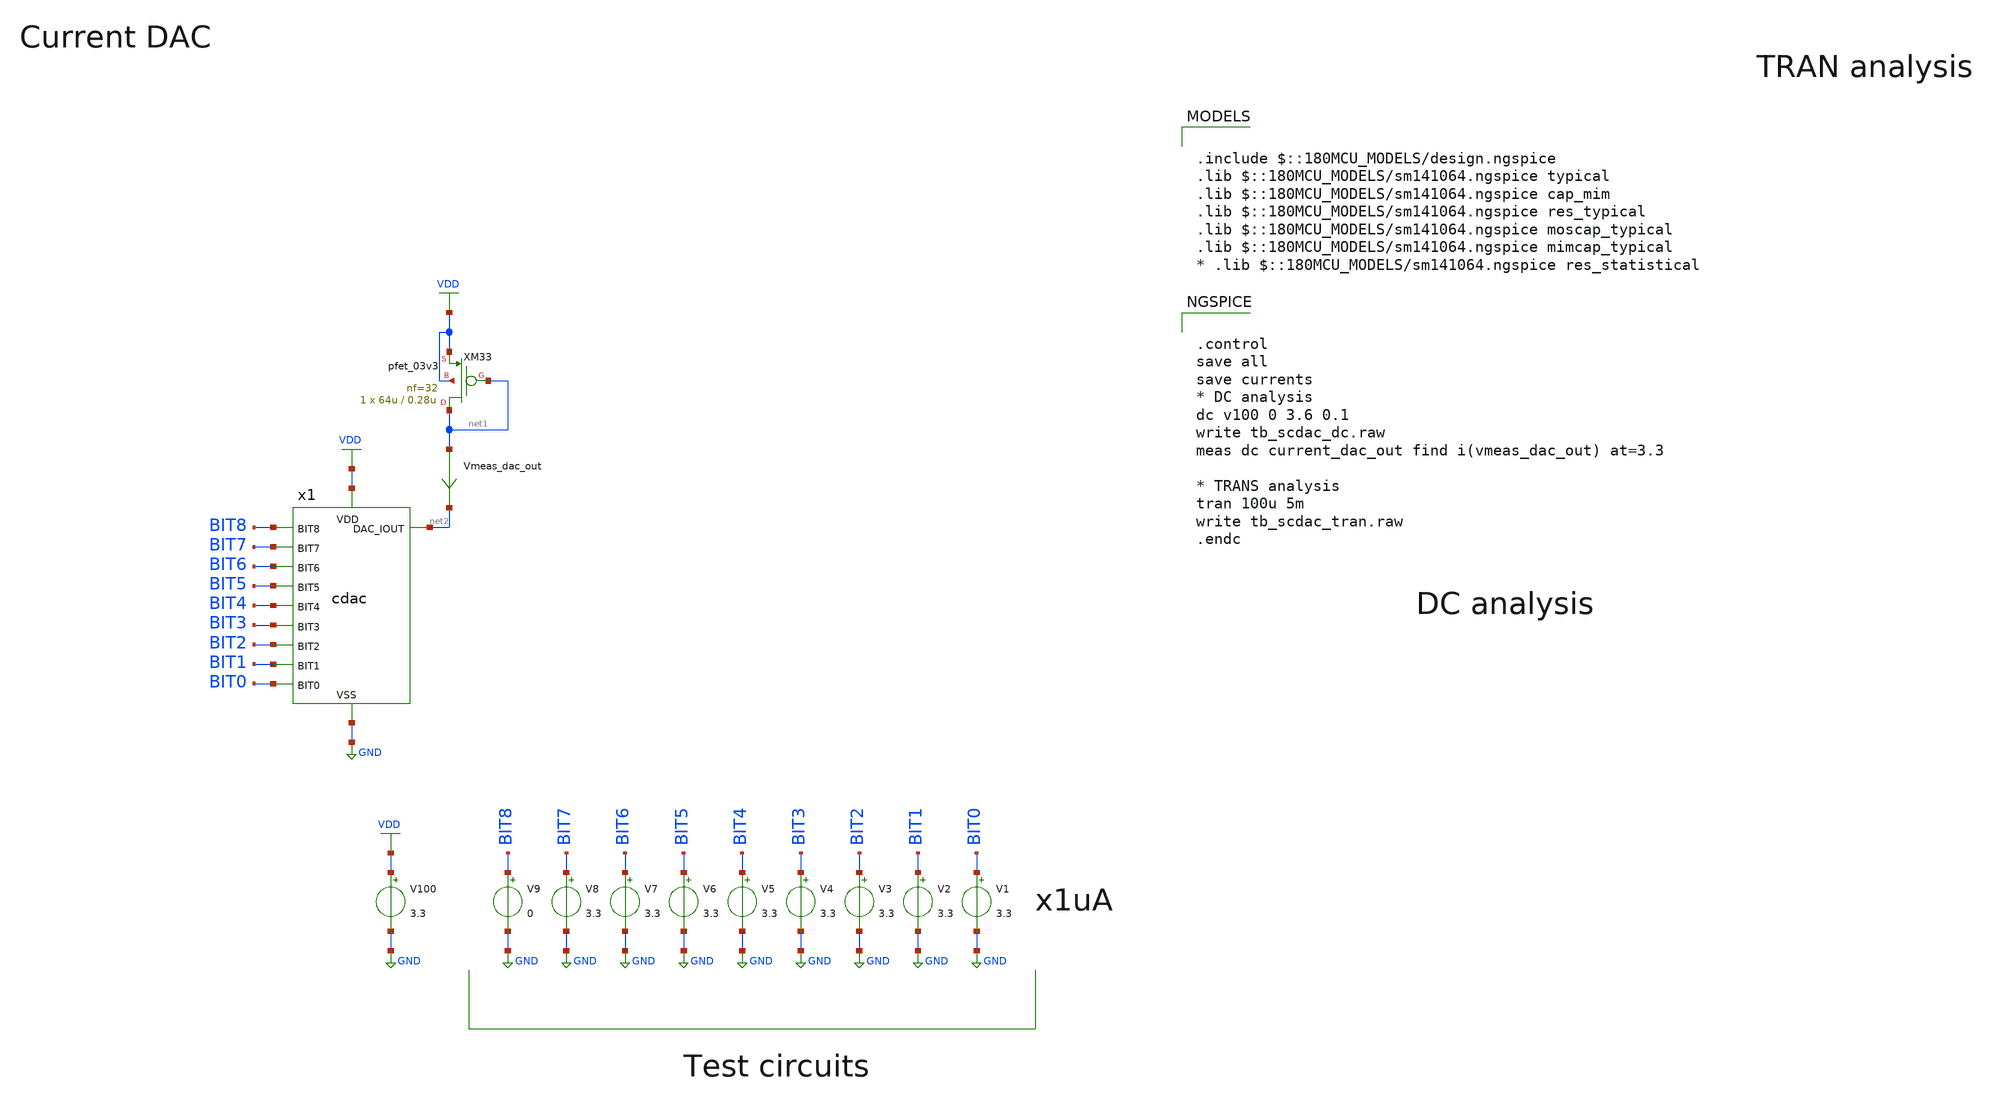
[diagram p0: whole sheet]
** sch_path: designs/libs/tb_analog/tb_scdac/tb_scdac.sch
* Copyright 2022 GlobalFoundries PDK Authors
* Licensed under the Apache License, Version 2.0 (the "License");
* you may not use this file except in compliance with the License.
* You may obtain a copy of the License at
* https://www.apache.org/licenses/LICENSE-2.0
* Unless required by applicable law or agreed to in writing, software
* distributed under the License is distributed on an "AS IS" BASIS,
* WITHOUT WARRANTIES OR CONDITIONS OF ANY KIND, either express or implied.
* See the License for the specific language governing permissions and
* limitations under the License.
**.subckt tb_scdac
V100 VDD GND 3.3
XM33 net1 net1 VDD VDD pfet_03v3 L=0.28u W=64u nf=32 ad='int((nf+1)/2) * W/nf * 0.18u' as='int((nf+2)/2) * W/nf * 0.18u'
+ pd='2*int((nf+1)/2) * (W/nf + 0.18u)' ps='2*int((nf+2)/2) * (W/nf + 0.18u)' nrd='0.18u / W' nrs='0.18u / W'
+ sa=0 sb=0 sd=0 m=1
Vmeas_dac_out net1 net2 0
.save i(vmeas_dac_out)
V8 BIT7 GND 3.3
V7 BIT6 GND 3.3
V6 BIT5 GND 3.3
V5 BIT4 GND 3.3
V4 BIT3 GND 3.3
V3 BIT2 GND 3.3
V2 BIT1 GND 3.3
V1 BIT0 GND 3.3
V9 BIT8 GND 0
x1 net2 GND VDD BIT8 BIT7 BIT6 BIT5 BIT4 BIT3 BIT2 BIT1 BIT0 cdac
**** begin user architecture code


.control
save all
save currents
* DC analysis
dc v100 0 3.6 0.1
write tb_scdac_dc.raw
meas dc current_dac_out find i(vmeas_dac_out) at=3.3

* TRANS analysis
tran 100u 5m
write tb_scdac_tran.raw
.endc



.include $::180MCU_MODELS/design.ngspice
.lib $::180MCU_MODELS/sm141064.ngspice typical
.lib $::180MCU_MODELS/sm141064.ngspice cap_mim
.lib $::180MCU_MODELS/sm141064.ngspice res_typical
.lib $::180MCU_MODELS/sm141064.ngspice moscap_typical
.lib $::180MCU_MODELS/sm141064.ngspice mimcap_typical
* .lib $::180MCU_MODELS/sm141064.ngspice res_statistical

**** end user architecture code
**.ends

* expanding   symbol:  libs/core_analog/scdac/cdac.sym # of pins=12
** sym_path: designs/libs/core_analog/scdac/cdac.sym
** sch_path: designs/libs/core_analog/scdac/cdac.sch
.subckt cdac DAC_IOUT VSS VDD BIT8 BIT7 BIT6 BIT5 BIT4 BIT3 BIT2 BIT1 BIT0
*.ipin BIT8
*.ipin BIT7
*.ipin BIT6
*.ipin BIT5
*.ipin BIT4
*.ipin BIT3
*.ipin BIT2
*.ipin BIT1
*.ipin BIT0
*.ipin VDD
*.ipin VSS
*.opin DAC_IOUT
XM8 64uA_REF 64uA_REF VSS VSS nfet_03v3 L=1u W=64u nf=1 ad='int((nf+1)/2) * W/nf * 0.18u' as='int((nf+2)/2) * W/nf * 0.18u'
+ pd='2*int((nf+1)/2) * (W/nf + 0.18u)' ps='2*int((nf+2)/2) * (W/nf + 0.18u)' nrd='0.18u / W' nrs='0.18u / W'
+ sa=0 sb=0 sd=0 m=1
XM11 net1 64uA_REF VSS VSS nfet_03v3 L=1u W=61.1u nf=1 ad='int((nf+1)/2) * W/nf * 0.18u' as='int((nf+2)/2) * W/nf * 0.18u'
+ pd='2*int((nf+1)/2) * (W/nf + 0.18u)' ps='2*int((nf+2)/2) * (W/nf + 0.18u)' nrd='0.18u / W' nrs='0.18u / W'
+ sa=0 sb=0 sd=0 m=1
XM13 DAC_IOUT BIT8 net1 VSS nfet_03v3 L=0.28u W=4u nf=1 ad='int((nf+1)/2) * W/nf * 0.18u' as='int((nf+2)/2) * W/nf * 0.18u'
+ pd='2*int((nf+1)/2) * (W/nf + 0.18u)' ps='2*int((nf+2)/2) * (W/nf + 0.18u)' nrd='0.18u / W' nrs='0.18u / W'
+ sa=0 sb=0 sd=0 m=1
XM15 net2 64uA_REF VSS VSS nfet_03v3 L=1u W=61.1u nf=1 ad='int((nf+1)/2) * W/nf * 0.18u' as='int((nf+2)/2) * W/nf * 0.18u'
+ pd='2*int((nf+1)/2) * (W/nf + 0.18u)' ps='2*int((nf+2)/2) * (W/nf + 0.18u)' nrd='0.18u / W' nrs='0.18u / W'
+ sa=0 sb=0 sd=0 m=1
XM16 DAC_IOUT BIT8 net2 VSS nfet_03v3 L=0.28u W=4u nf=1 ad='int((nf+1)/2) * W/nf * 0.18u' as='int((nf+2)/2) * W/nf * 0.18u'
+ pd='2*int((nf+1)/2) * (W/nf + 0.18u)' ps='2*int((nf+2)/2) * (W/nf + 0.18u)' nrd='0.18u / W' nrs='0.18u / W'
+ sa=0 sb=0 sd=0 m=1
XM18 net3 64uA_REF VSS VSS nfet_03v3 L=1u W=61.1u nf=1 ad='int((nf+1)/2) * W/nf * 0.18u' as='int((nf+2)/2) * W/nf * 0.18u'
+ pd='2*int((nf+1)/2) * (W/nf + 0.18u)' ps='2*int((nf+2)/2) * (W/nf + 0.18u)' nrd='0.18u / W' nrs='0.18u / W'
+ sa=0 sb=0 sd=0 m=1
XM19 DAC_IOUT BIT8 net3 VSS nfet_03v3 L=0.28u W=4u nf=1 ad='int((nf+1)/2) * W/nf * 0.18u' as='int((nf+2)/2) * W/nf * 0.18u'
+ pd='2*int((nf+1)/2) * (W/nf + 0.18u)' ps='2*int((nf+2)/2) * (W/nf + 0.18u)' nrd='0.18u / W' nrs='0.18u / W'
+ sa=0 sb=0 sd=0 m=1
XM21 net4 64uA_REF VSS VSS nfet_03v3 L=1u W=61.1u nf=1 ad='int((nf+1)/2) * W/nf * 0.18u' as='int((nf+2)/2) * W/nf * 0.18u'
+ pd='2*int((nf+1)/2) * (W/nf + 0.18u)' ps='2*int((nf+2)/2) * (W/nf + 0.18u)' nrd='0.18u / W' nrs='0.18u / W'
+ sa=0 sb=0 sd=0 m=1
XM22 DAC_IOUT BIT8 net4 VSS nfet_03v3 L=0.28u W=4u nf=1 ad='int((nf+1)/2) * W/nf * 0.18u' as='int((nf+2)/2) * W/nf * 0.18u'
+ pd='2*int((nf+1)/2) * (W/nf + 0.18u)' ps='2*int((nf+2)/2) * (W/nf + 0.18u)' nrd='0.18u / W' nrs='0.18u / W'
+ sa=0 sb=0 sd=0 m=1
XM24 net5 64uA_REF VSS VSS nfet_03v3 L=1u W=61.1u nf=1 ad='int((nf+1)/2) * W/nf * 0.18u' as='int((nf+2)/2) * W/nf * 0.18u'
+ pd='2*int((nf+1)/2) * (W/nf + 0.18u)' ps='2*int((nf+2)/2) * (W/nf + 0.18u)' nrd='0.18u / W' nrs='0.18u / W'
+ sa=0 sb=0 sd=0 m=1
XM25 DAC_IOUT BIT7 net5 VSS nfet_03v3 L=0.28u W=4u nf=1 ad='int((nf+1)/2) * W/nf * 0.18u' as='int((nf+2)/2) * W/nf * 0.18u'
+ pd='2*int((nf+1)/2) * (W/nf + 0.18u)' ps='2*int((nf+2)/2) * (W/nf + 0.18u)' nrd='0.18u / W' nrs='0.18u / W'
+ sa=0 sb=0 sd=0 m=1
XM27 net6 64uA_REF VSS VSS nfet_03v3 L=1u W=61.1u nf=1 ad='int((nf+1)/2) * W/nf * 0.18u' as='int((nf+2)/2) * W/nf * 0.18u'
+ pd='2*int((nf+1)/2) * (W/nf + 0.18u)' ps='2*int((nf+2)/2) * (W/nf + 0.18u)' nrd='0.18u / W' nrs='0.18u / W'
+ sa=0 sb=0 sd=0 m=1
XM28 DAC_IOUT BIT7 net6 VSS nfet_03v3 L=0.28u W=4u nf=1 ad='int((nf+1)/2) * W/nf * 0.18u' as='int((nf+2)/2) * W/nf * 0.18u'
+ pd='2*int((nf+1)/2) * (W/nf + 0.18u)' ps='2*int((nf+2)/2) * (W/nf + 0.18u)' nrd='0.18u / W' nrs='0.18u / W'
+ sa=0 sb=0 sd=0 m=1
XM30 net7 64uA_REF VSS VSS nfet_03v3 L=1u W=61.1u nf=1 ad='int((nf+1)/2) * W/nf * 0.18u' as='int((nf+2)/2) * W/nf * 0.18u'
+ pd='2*int((nf+1)/2) * (W/nf + 0.18u)' ps='2*int((nf+2)/2) * (W/nf + 0.18u)' nrd='0.18u / W' nrs='0.18u / W'
+ sa=0 sb=0 sd=0 m=1
XM31 DAC_IOUT BIT6 net7 VSS nfet_03v3 L=0.28u W=4u nf=8 ad='int((nf+1)/2) * W/nf * 0.18u' as='int((nf+2)/2) * W/nf * 0.18u'
+ pd='2*int((nf+1)/2) * (W/nf + 0.18u)' ps='2*int((nf+2)/2) * (W/nf + 0.18u)' nrd='0.18u / W' nrs='0.18u / W'
+ sa=0 sb=0 sd=0 m=1
XM1 net8 64uA_REF VSS VSS nfet_03v3 L=1u W=7.62u nf=1 ad='int((nf+1)/2) * W/nf * 0.18u' as='int((nf+2)/2) * W/nf * 0.18u'
+ pd='2*int((nf+1)/2) * (W/nf + 0.18u)' ps='2*int((nf+2)/2) * (W/nf + 0.18u)' nrd='0.18u / W' nrs='0.18u / W'
+ sa=0 sb=0 sd=0 m=1
XM2 DAC_IOUT BIT5 net8 VSS nfet_03v3 L=0.28u W=4u nf=1 ad='int((nf+1)/2) * W/nf * 0.18u' as='int((nf+2)/2) * W/nf * 0.18u'
+ pd='2*int((nf+1)/2) * (W/nf + 0.18u)' ps='2*int((nf+2)/2) * (W/nf + 0.18u)' nrd='0.18u / W' nrs='0.18u / W'
+ sa=0 sb=0 sd=0 m=1
XM3 net9 64uA_REF VSS VSS nfet_03v3 L=1u W=7.62u nf=1 ad='int((nf+1)/2) * W/nf * 0.18u' as='int((nf+2)/2) * W/nf * 0.18u'
+ pd='2*int((nf+1)/2) * (W/nf + 0.18u)' ps='2*int((nf+2)/2) * (W/nf + 0.18u)' nrd='0.18u / W' nrs='0.18u / W'
+ sa=0 sb=0 sd=0 m=1
XM4 DAC_IOUT BIT5 net9 VSS nfet_03v3 L=0.28u W=4u nf=1 ad='int((nf+1)/2) * W/nf * 0.18u' as='int((nf+2)/2) * W/nf * 0.18u'
+ pd='2*int((nf+1)/2) * (W/nf + 0.18u)' ps='2*int((nf+2)/2) * (W/nf + 0.18u)' nrd='0.18u / W' nrs='0.18u / W'
+ sa=0 sb=0 sd=0 m=1
XM5 net10 64uA_REF VSS VSS nfet_03v3 L=1u W=7.62u nf=1 ad='int((nf+1)/2) * W/nf * 0.18u' as='int((nf+2)/2) * W/nf * 0.18u'
+ pd='2*int((nf+1)/2) * (W/nf + 0.18u)' ps='2*int((nf+2)/2) * (W/nf + 0.18u)' nrd='0.18u / W' nrs='0.18u / W'
+ sa=0 sb=0 sd=0 m=1
XM6 DAC_IOUT BIT5 net10 VSS nfet_03v3 L=0.28u W=4u nf=1 ad='int((nf+1)/2) * W/nf * 0.18u' as='int((nf+2)/2) * W/nf * 0.18u'
+ pd='2*int((nf+1)/2) * (W/nf + 0.18u)' ps='2*int((nf+2)/2) * (W/nf + 0.18u)' nrd='0.18u / W' nrs='0.18u / W'
+ sa=0 sb=0 sd=0 m=1
XM7 net11 64uA_REF VSS VSS nfet_03v3 L=1u W=7.62u nf=1 ad='int((nf+1)/2) * W/nf * 0.18u' as='int((nf+2)/2) * W/nf * 0.18u'
+ pd='2*int((nf+1)/2) * (W/nf + 0.18u)' ps='2*int((nf+2)/2) * (W/nf + 0.18u)' nrd='0.18u / W' nrs='0.18u / W'
+ sa=0 sb=0 sd=0 m=1
XM9 DAC_IOUT BIT5 net11 VSS nfet_03v3 L=0.28u W=4u nf=1 ad='int((nf+1)/2) * W/nf * 0.18u' as='int((nf+2)/2) * W/nf * 0.18u'
+ pd='2*int((nf+1)/2) * (W/nf + 0.18u)' ps='2*int((nf+2)/2) * (W/nf + 0.18u)' nrd='0.18u / W' nrs='0.18u / W'
+ sa=0 sb=0 sd=0 m=1
XM10 net12 64uA_REF VSS VSS nfet_03v3 L=1u W=7.62u nf=1 ad='int((nf+1)/2) * W/nf * 0.18u' as='int((nf+2)/2) * W/nf * 0.18u'
+ pd='2*int((nf+1)/2) * (W/nf + 0.18u)' ps='2*int((nf+2)/2) * (W/nf + 0.18u)' nrd='0.18u / W' nrs='0.18u / W'
+ sa=0 sb=0 sd=0 m=1
XM12 DAC_IOUT BIT4 net12 VSS nfet_03v3 L=0.28u W=4u nf=1 ad='int((nf+1)/2) * W/nf * 0.18u' as='int((nf+2)/2) * W/nf * 0.18u'
+ pd='2*int((nf+1)/2) * (W/nf + 0.18u)' ps='2*int((nf+2)/2) * (W/nf + 0.18u)' nrd='0.18u / W' nrs='0.18u / W'
+ sa=0 sb=0 sd=0 m=1
XM14 net13 64uA_REF VSS VSS nfet_03v3 L=1u W=7.62u nf=1 ad='int((nf+1)/2) * W/nf * 0.18u' as='int((nf+2)/2) * W/nf * 0.18u'
+ pd='2*int((nf+1)/2) * (W/nf + 0.18u)' ps='2*int((nf+2)/2) * (W/nf + 0.18u)' nrd='0.18u / W' nrs='0.18u / W'
+ sa=0 sb=0 sd=0 m=1
XM17 DAC_IOUT BIT4 net13 VSS nfet_03v3 L=0.28u W=4u nf=1 ad='int((nf+1)/2) * W/nf * 0.18u' as='int((nf+2)/2) * W/nf * 0.18u'
+ pd='2*int((nf+1)/2) * (W/nf + 0.18u)' ps='2*int((nf+2)/2) * (W/nf + 0.18u)' nrd='0.18u / W' nrs='0.18u / W'
+ sa=0 sb=0 sd=0 m=1
XM20 net14 64uA_REF VSS VSS nfet_03v3 L=1u W=7.62u nf=1 ad='int((nf+1)/2) * W/nf * 0.18u' as='int((nf+2)/2) * W/nf * 0.18u'
+ pd='2*int((nf+1)/2) * (W/nf + 0.18u)' ps='2*int((nf+2)/2) * (W/nf + 0.18u)' nrd='0.18u / W' nrs='0.18u / W'
+ sa=0 sb=0 sd=0 m=1
XM23 DAC_IOUT BIT3 net14 VSS nfet_03v3 L=0.28u W=4u nf=1 ad='int((nf+1)/2) * W/nf * 0.18u' as='int((nf+2)/2) * W/nf * 0.18u'
+ pd='2*int((nf+1)/2) * (W/nf + 0.18u)' ps='2*int((nf+2)/2) * (W/nf + 0.18u)' nrd='0.18u / W' nrs='0.18u / W'
+ sa=0 sb=0 sd=0 m=1
XM26 net15 64uA_REF VSS VSS nfet_03v3 L=1u W=1.01u nf=1 ad='int((nf+1)/2) * W/nf * 0.18u' as='int((nf+2)/2) * W/nf * 0.18u'
+ pd='2*int((nf+1)/2) * (W/nf + 0.18u)' ps='2*int((nf+2)/2) * (W/nf + 0.18u)' nrd='0.18u / W' nrs='0.18u / W'
+ sa=0 sb=0 sd=0 m=1
XM29 DAC_IOUT BIT2 net15 VSS nfet_03v3 L=0.28u W=4u nf=1 ad='int((nf+1)/2) * W/nf * 0.18u' as='int((nf+2)/2) * W/nf * 0.18u'
+ pd='2*int((nf+1)/2) * (W/nf + 0.18u)' ps='2*int((nf+2)/2) * (W/nf + 0.18u)' nrd='0.18u / W' nrs='0.18u / W'
+ sa=0 sb=0 sd=0 m=1
XM32 net16 64uA_REF VSS VSS nfet_03v3 L=1u W=1.01u nf=1 ad='int((nf+1)/2) * W/nf * 0.18u' as='int((nf+2)/2) * W/nf * 0.18u'
+ pd='2*int((nf+1)/2) * (W/nf + 0.18u)' ps='2*int((nf+2)/2) * (W/nf + 0.18u)' nrd='0.18u / W' nrs='0.18u / W'
+ sa=0 sb=0 sd=0 m=1
XM35 DAC_IOUT BIT2 net16 VSS nfet_03v3 L=0.28u W=4u nf=1 ad='int((nf+1)/2) * W/nf * 0.18u' as='int((nf+2)/2) * W/nf * 0.18u'
+ pd='2*int((nf+1)/2) * (W/nf + 0.18u)' ps='2*int((nf+2)/2) * (W/nf + 0.18u)' nrd='0.18u / W' nrs='0.18u / W'
+ sa=0 sb=0 sd=0 m=1
XM36 net17 64uA_REF VSS VSS nfet_03v3 L=1u W=1.01u nf=1 ad='int((nf+1)/2) * W/nf * 0.18u' as='int((nf+2)/2) * W/nf * 0.18u'
+ pd='2*int((nf+1)/2) * (W/nf + 0.18u)' ps='2*int((nf+2)/2) * (W/nf + 0.18u)' nrd='0.18u / W' nrs='0.18u / W'
+ sa=0 sb=0 sd=0 m=1
XM37 DAC_IOUT BIT2 net17 VSS nfet_03v3 L=0.28u W=4u nf=1 ad='int((nf+1)/2) * W/nf * 0.18u' as='int((nf+2)/2) * W/nf * 0.18u'
+ pd='2*int((nf+1)/2) * (W/nf + 0.18u)' ps='2*int((nf+2)/2) * (W/nf + 0.18u)' nrd='0.18u / W' nrs='0.18u / W'
+ sa=0 sb=0 sd=0 m=1
XM38 net18 64uA_REF VSS VSS nfet_03v3 L=1u W=1.01u nf=1 ad='int((nf+1)/2) * W/nf * 0.18u' as='int((nf+2)/2) * W/nf * 0.18u'
+ pd='2*int((nf+1)/2) * (W/nf + 0.18u)' ps='2*int((nf+2)/2) * (W/nf + 0.18u)' nrd='0.18u / W' nrs='0.18u / W'
+ sa=0 sb=0 sd=0 m=1
XM39 DAC_IOUT BIT2 net18 VSS nfet_03v3 L=0.28u W=4u nf=1 ad='int((nf+1)/2) * W/nf * 0.18u' as='int((nf+2)/2) * W/nf * 0.18u'
+ pd='2*int((nf+1)/2) * (W/nf + 0.18u)' ps='2*int((nf+2)/2) * (W/nf + 0.18u)' nrd='0.18u / W' nrs='0.18u / W'
+ sa=0 sb=0 sd=0 m=1
XM40 net19 64uA_REF VSS VSS nfet_03v3 L=1u W=1.01u nf=1 ad='int((nf+1)/2) * W/nf * 0.18u' as='int((nf+2)/2) * W/nf * 0.18u'
+ pd='2*int((nf+1)/2) * (W/nf + 0.18u)' ps='2*int((nf+2)/2) * (W/nf + 0.18u)' nrd='0.18u / W' nrs='0.18u / W'
+ sa=0 sb=0 sd=0 m=1
XM41 DAC_IOUT BIT1 net19 VSS nfet_03v3 L=0.28u W=4u nf=1 ad='int((nf+1)/2) * W/nf * 0.18u' as='int((nf+2)/2) * W/nf * 0.18u'
+ pd='2*int((nf+1)/2) * (W/nf + 0.18u)' ps='2*int((nf+2)/2) * (W/nf + 0.18u)' nrd='0.18u / W' nrs='0.18u / W'
+ sa=0 sb=0 sd=0 m=1
XM42 net20 64uA_REF VSS VSS nfet_03v3 L=1u W=1.01u nf=1 ad='int((nf+1)/2) * W/nf * 0.18u' as='int((nf+2)/2) * W/nf * 0.18u'
+ pd='2*int((nf+1)/2) * (W/nf + 0.18u)' ps='2*int((nf+2)/2) * (W/nf + 0.18u)' nrd='0.18u / W' nrs='0.18u / W'
+ sa=0 sb=0 sd=0 m=1
XM43 DAC_IOUT BIT1 net20 VSS nfet_03v3 L=0.28u W=4u nf=1 ad='int((nf+1)/2) * W/nf * 0.18u' as='int((nf+2)/2) * W/nf * 0.18u'
+ pd='2*int((nf+1)/2) * (W/nf + 0.18u)' ps='2*int((nf+2)/2) * (W/nf + 0.18u)' nrd='0.18u / W' nrs='0.18u / W'
+ sa=0 sb=0 sd=0 m=1
XM44 net21 64uA_REF VSS VSS nfet_03v3 L=1u W=1.01u nf=1 ad='int((nf+1)/2) * W/nf * 0.18u' as='int((nf+2)/2) * W/nf * 0.18u'
+ pd='2*int((nf+1)/2) * (W/nf + 0.18u)' ps='2*int((nf+2)/2) * (W/nf + 0.18u)' nrd='0.18u / W' nrs='0.18u / W'
+ sa=0 sb=0 sd=0 m=1
XM45 DAC_IOUT BIT0 net21 VSS nfet_03v3 L=0.28u W=4u nf=1 ad='int((nf+1)/2) * W/nf * 0.18u' as='int((nf+2)/2) * W/nf * 0.18u'
+ pd='2*int((nf+1)/2) * (W/nf + 0.18u)' ps='2*int((nf+2)/2) * (W/nf + 0.18u)' nrd='0.18u / W' nrs='0.18u / W'
+ sa=0 sb=0 sd=0 m=1
x1 VDD VSS 64uA_REF bmr
.ends


* expanding   symbol:  libs/core_analog/bmr/bmr.sym # of pins=3
** sym_path: designs/libs/core_analog/bmr/bmr.sym
** sch_path: designs/libs/core_analog/bmr/bmr.sch
.subckt bmr VDD VSS 64uA_OUT
*.ipin VDD
*.ipin VSS
*.opin 64uA_OUT
XM3 net2 net1 net3 VSS nfet_03v3 L=1u W=10u nf=1 ad='int((nf+1)/2) * W/nf * 0.18u' as='int((nf+2)/2) * W/nf * 0.18u'
+ pd='2*int((nf+1)/2) * (W/nf + 0.18u)' ps='2*int((nf+2)/2) * (W/nf + 0.18u)' nrd='0.18u / W' nrs='0.18u / W'
+ sa=0 sb=0 sd=0 m=1
XM5 net3 net2 VDD VDD pfet_03v3 L=3u W=15u nf=1 ad='int((nf+1)/2) * W/nf * 0.18u' as='int((nf+2)/2) * W/nf * 0.18u'
+ pd='2*int((nf+1)/2) * (W/nf + 0.18u)' ps='2*int((nf+2)/2) * (W/nf + 0.18u)' nrd='0.18u / W' nrs='0.18u / W'
+ sa=0 sb=0 sd=0 m=1
XM6 net1 net1 VDD VDD pfet_03v3 L=4u W=4u nf=1 ad='int((nf+1)/2) * W/nf * 0.18u' as='int((nf+2)/2) * W/nf * 0.18u'
+ pd='2*int((nf+1)/2) * (W/nf + 0.18u)' ps='2*int((nf+2)/2) * (W/nf + 0.18u)' nrd='0.18u / W' nrs='0.18u / W'
+ sa=0 sb=0 sd=0 m=1
XM9 net2 net3 net4 VSS nfet_03v3 L=3u W=10u nf=1 ad='int((nf+1)/2) * W/nf * 0.18u' as='int((nf+2)/2) * W/nf * 0.18u'
+ pd='2*int((nf+1)/2) * (W/nf + 0.18u)' ps='2*int((nf+2)/2) * (W/nf + 0.18u)' nrd='0.18u / W' nrs='0.18u / W'
+ sa=0 sb=0 sd=0 m=1
XM12 net2 net2 VDD VDD pfet_03v3 L=3u W=15u nf=1 ad='int((nf+1)/2) * W/nf * 0.18u' as='int((nf+2)/2) * W/nf * 0.18u'
+ pd='2*int((nf+1)/2) * (W/nf + 0.18u)' ps='2*int((nf+2)/2) * (W/nf + 0.18u)' nrd='0.18u / W' nrs='0.18u / W'
+ sa=0 sb=0 sd=0 m=1
XM1 net1 net3 VSS VSS nfet_03v3 L=3u W=10u nf=1 ad='int((nf+1)/2) * W/nf * 0.18u' as='int((nf+2)/2) * W/nf * 0.18u'
+ pd='2*int((nf+1)/2) * (W/nf + 0.18u)' ps='2*int((nf+2)/2) * (W/nf + 0.18u)' nrd='0.18u / W' nrs='0.18u / W'
+ sa=0 sb=0 sd=0 m=1
XM2 net3 net3 VSS VSS nfet_03v3 L=3u W=5u nf=1 ad='int((nf+1)/2) * W/nf * 0.18u' as='int((nf+2)/2) * W/nf * 0.18u'
+ pd='2*int((nf+1)/2) * (W/nf + 0.18u)' ps='2*int((nf+2)/2) * (W/nf + 0.18u)' nrd='0.18u / W' nrs='0.18u / W'
+ sa=0 sb=0 sd=0 m=1
XM4 64uA_OUT net2 VDD VDD pfet_03v3 L=3u W=15u nf=1 ad='int((nf+1)/2) * W/nf * 0.18u' as='int((nf+2)/2) * W/nf * 0.18u'
+ pd='2*int((nf+1)/2) * (W/nf + 0.18u)' ps='2*int((nf+2)/2) * (W/nf + 0.18u)' nrd='0.18u / W' nrs='0.18u / W'
+ sa=0 sb=0 sd=0 m=1
XR2 VSS net4 VDD ppolyf_u_1k r_width=1e-6 r_length=2.61e-6 m=1
.ends

.GLOBAL VDD
.GLOBAL GND
.end
